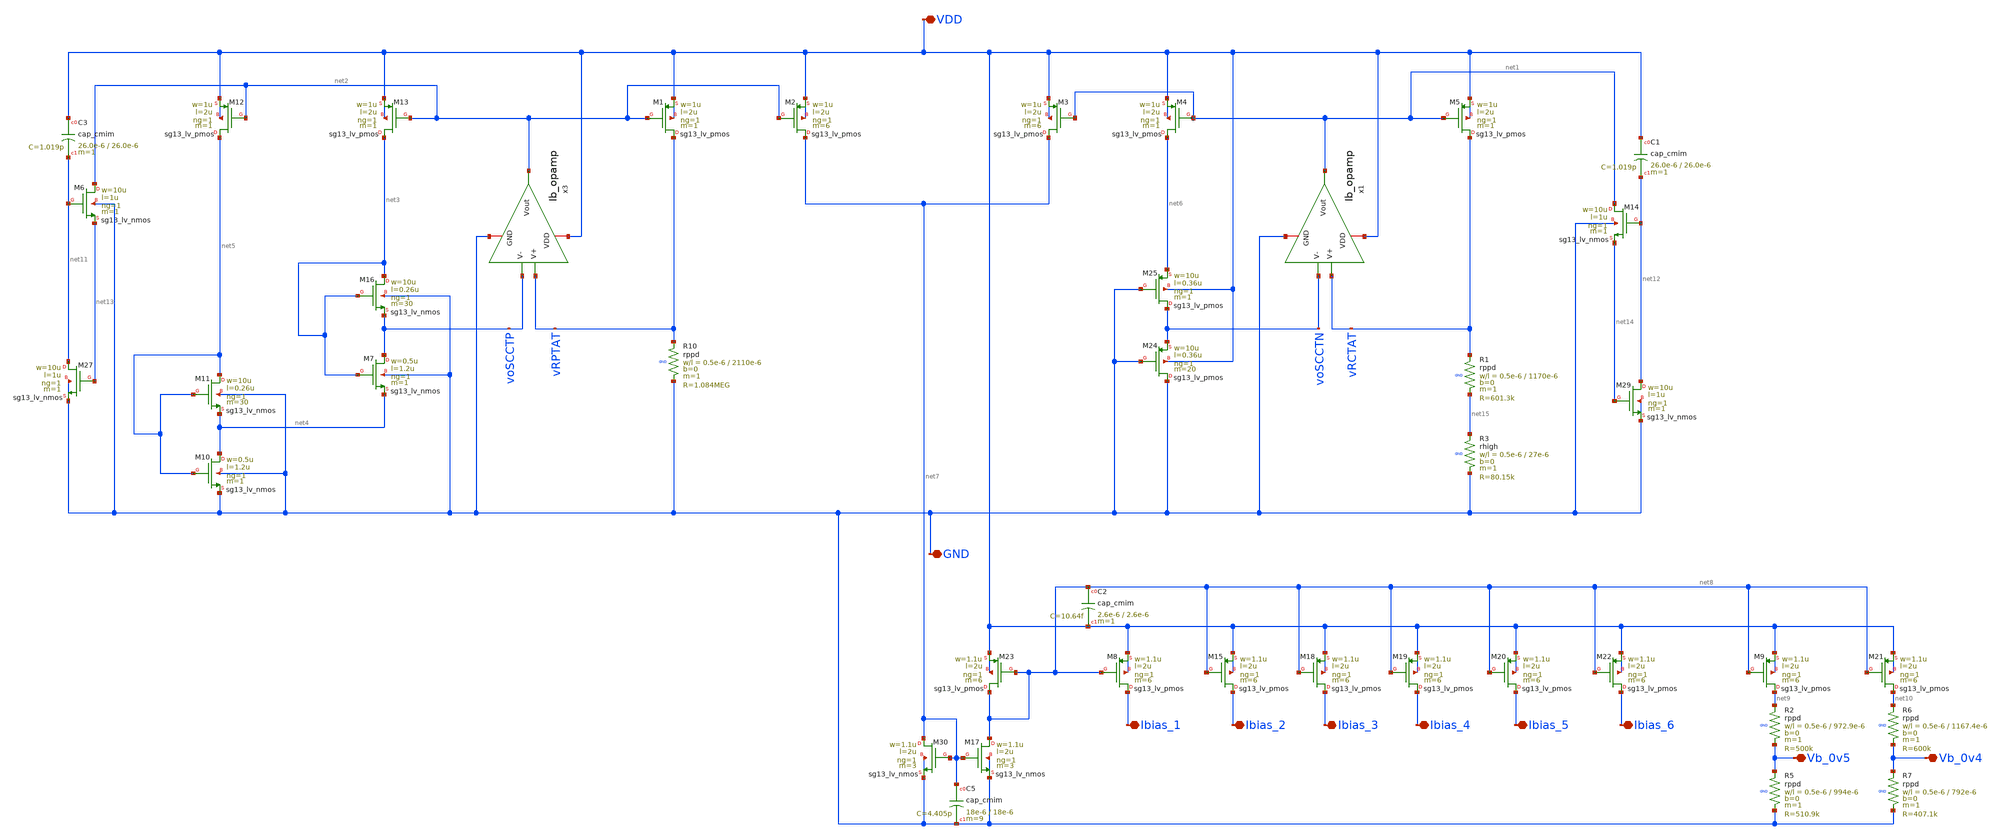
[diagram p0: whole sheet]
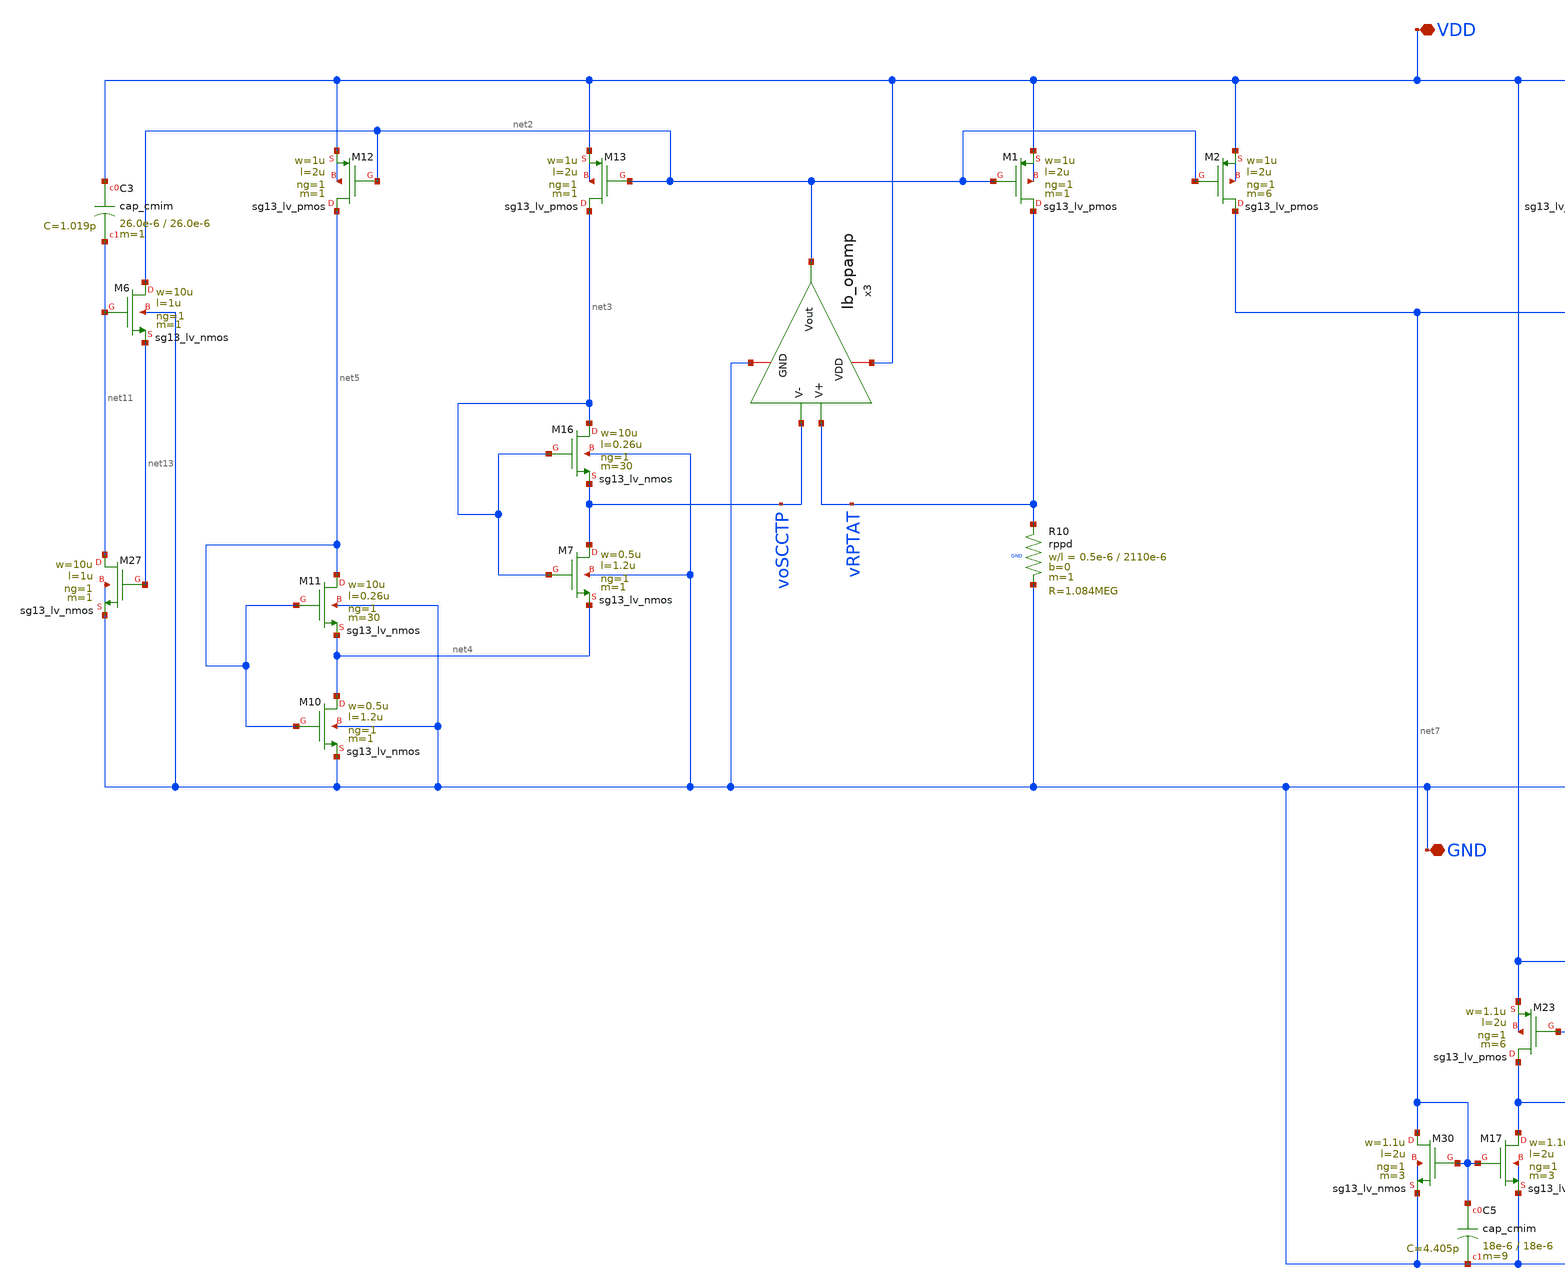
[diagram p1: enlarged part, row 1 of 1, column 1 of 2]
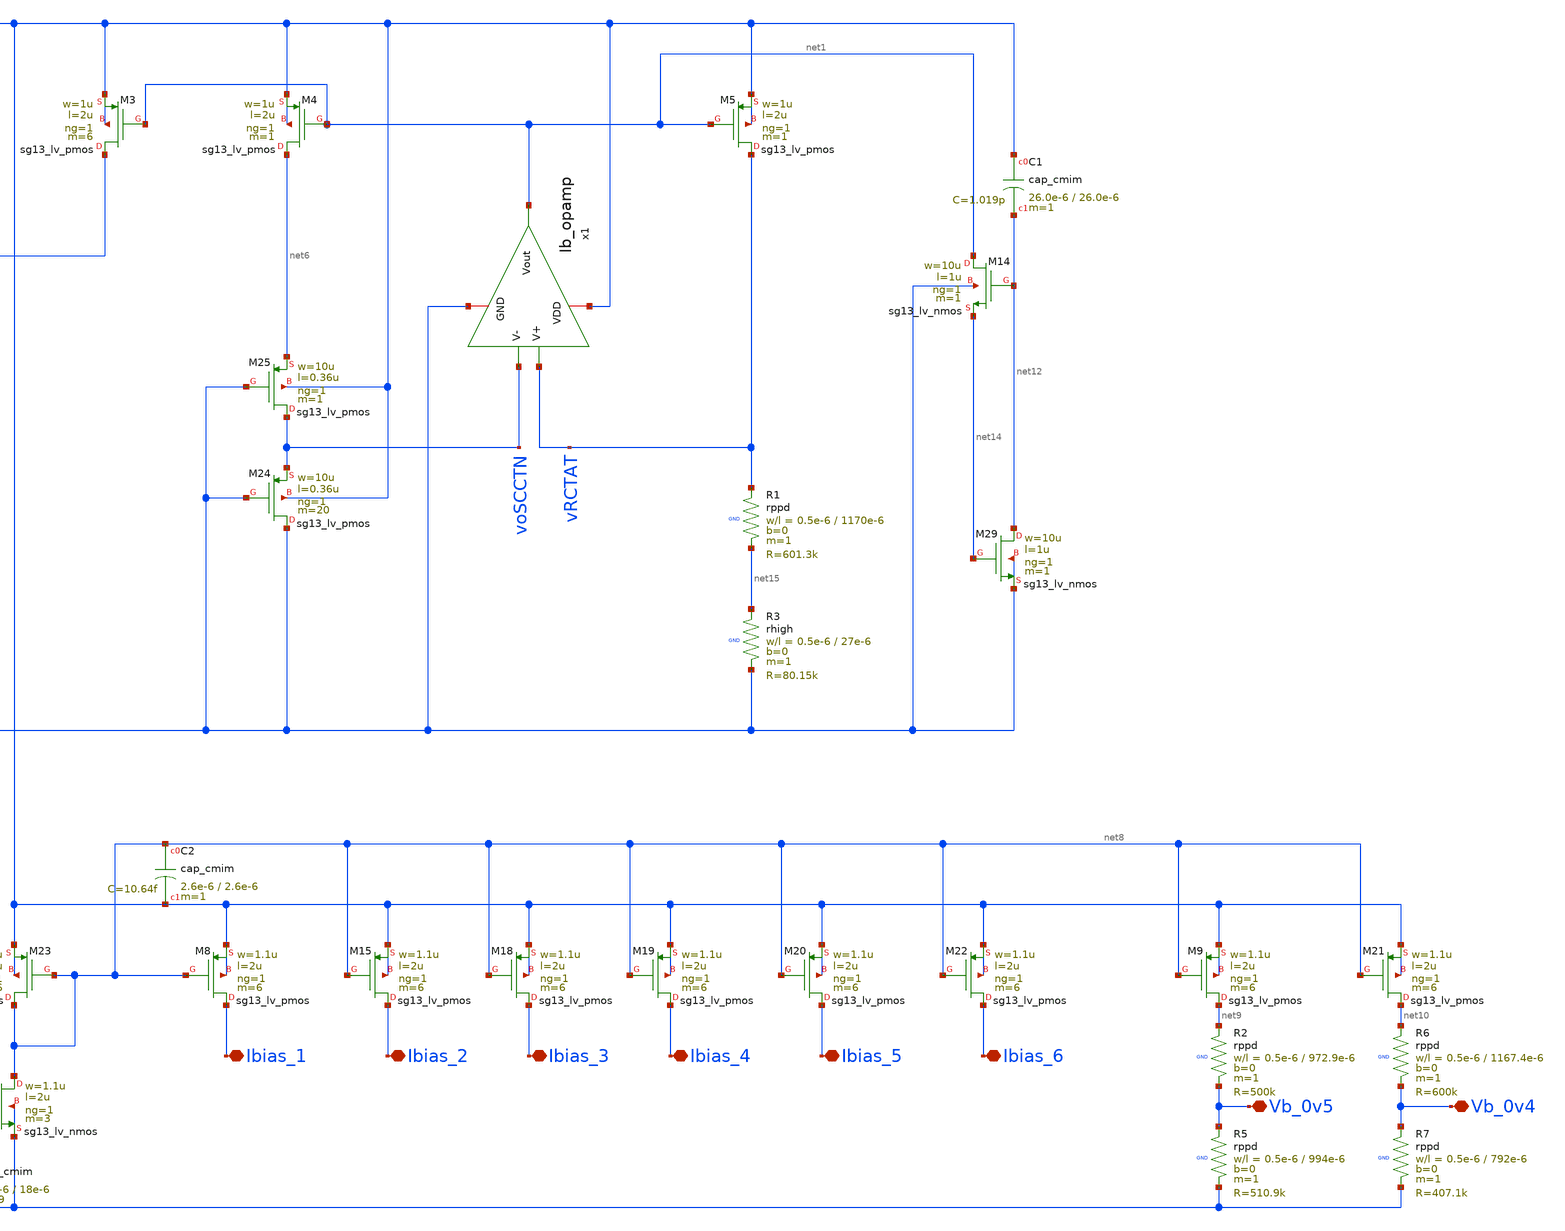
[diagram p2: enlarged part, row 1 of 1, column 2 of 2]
** sch_path: SSDOR_1.2V_v3/components/Ibias_uA/CTAT_PTAT/CTAT_PTAT.sch
**.subckt CTAT_PTAT VDD GND Ibias_1 Ibias_2 Ibias_3 Ibias_4 Ibias_5 Ibias_6 Vb_0v4 Vb_0v5
*.iopin VDD
*.iopin GND
*.iopin Ibias_1
*.iopin Ibias_2
*.iopin Ibias_3
*.iopin Ibias_4
*.iopin Ibias_5
*.iopin Ibias_6
*.iopin Vb_0v4
*.iopin Vb_0v5
XM1 vRPTAT net2 VDD VDD sg13_lv_pmos w=1u l=2u ng=1 m=1 mm_ok=1
XM2 net7 net2 VDD VDD sg13_lv_pmos w=1u l=2u ng=1 m=6 mm_ok=1
XM3 net7 net1 VDD VDD sg13_lv_pmos w=1u l=2u ng=1 m=6 mm_ok=1
XM4 net6 net1 VDD VDD sg13_lv_pmos w=1u l=2u ng=1 m=1 mm_ok=1
XM12 net5 net2 VDD VDD sg13_lv_pmos w=1u l=2u ng=1 m=1 mm_ok=1
XM13 net3 net2 VDD VDD sg13_lv_pmos w=1u l=2u ng=1 m=1 mm_ok=1
XM5 vRCTAT net1 VDD VDD sg13_lv_pmos w=1u l=2u ng=1 m=1 mm_ok=1
XM7 voSCCTP net3 net4 GND sg13_lv_nmos w=0.5u l=1.2u ng=1 m=1 mm_ok=1
XM10 net4 net5 GND GND sg13_lv_nmos w=0.5u l=1.2u ng=1 m=1 mm_ok=1
XM11 net5 net5 net4 GND sg13_lv_nmos w=10u l=0.26u ng=1 m=30 mm_ok=1
XM16 net3 net3 voSCCTP GND sg13_lv_nmos w=10u l=0.26u ng=1 m=30 mm_ok=1
XM30 net7 net7 GND GND sg13_lv_nmos w=1.1u l=2u ng=1 m=3 mm_ok=1
XR2 net9 Vb_0v5 GND rppd w=0.5e-6 l=972.9e-6 m=1 b=0 mm_ok=1
XR6 net10 Vb_0v4 GND rppd w=0.5e-6 l=1167.4e-6 m=1 b=0 mm_ok=1
XR7 Vb_0v4 GND GND rppd w=0.5e-6 l=792e-6 m=1 b=0 mm_ok=1
XR5 Vb_0v5 GND GND rppd w=0.5e-6 l=994e-6 m=1 b=0 mm_ok=1
XM17 net8 net7 GND GND sg13_lv_nmos w=1.1u l=2u ng=1 m=3 mm_ok=1
XM23 net8 net8 VDD VDD sg13_lv_pmos w=1.1u l=2u ng=1 m=6 mm_ok=1
XM8 Ibias_1 net8 VDD VDD sg13_lv_pmos w=1.1u l=2u ng=1 m=6 mm_ok=1
XM15 Ibias_2 net8 VDD VDD sg13_lv_pmos w=1.1u l=2u ng=1 m=6 mm_ok=1
XM18 Ibias_3 net8 VDD VDD sg13_lv_pmos w=1.1u l=2u ng=1 m=6 mm_ok=1
XM19 Ibias_4 net8 VDD VDD sg13_lv_pmos w=1.1u l=2u ng=1 m=6 mm_ok=1
XM20 Ibias_5 net8 VDD VDD sg13_lv_pmos w=1.1u l=2u ng=1 m=6 mm_ok=1
XM22 Ibias_6 net8 VDD VDD sg13_lv_pmos w=1.1u l=2u ng=1 m=6 mm_ok=1
XM24 GND GND voSCCTN VDD sg13_lv_pmos w=10u l=0.36u ng=1 m=20 mm_ok=1
XM25 voSCCTN GND net6 VDD sg13_lv_pmos w=10u l=0.36u ng=1 m=1 mm_ok=1
XM27 net11 net13 GND GND sg13_lv_nmos w=10u l=1u ng=1 m=1 mm_ok=1
XM29 net12 net14 GND GND sg13_lv_nmos w=10u l=1u ng=1 m=1 mm_ok=1
XR1 vRCTAT net15 GND rppd w=0.5e-6 l=1170e-6 m=1 b=0 mm_ok=1
XR3 net15 GND GND rhigh w=0.5e-6 l=27e-6 m=1 b=0 mm_ok=1
XR10 vRPTAT GND GND rppd w=0.5e-6 l=2110e-6 m=1 b=0 mm_ok=1
XC3 VDD net11 cap_cmim w=26.0e-6 l=26.0e-6 m=1 mm_ok=1
XC1 VDD net12 cap_cmim w=26.0e-6 l=26.0e-6 m=1 mm_ok=1
XM6 net2 net11 net13 GND sg13_lv_nmos w=10u l=1u ng=1 m=1 mm_ok=1
XM14 net1 net12 net14 GND sg13_lv_nmos w=10u l=1u ng=1 m=1 mm_ok=1
x3 VDD net2 voSCCTP vRPTAT GND Ib_opamp
x1 VDD net1 voSCCTN vRCTAT GND Ib_opamp
XC5 net7 GND cap_cmim w=18e-6 l=18e-6 m=9 mm_ok=1
XC2 net8 VDD cap_cmim w=2.6e-6 l=2.6e-6 m=1 mm_ok=1
XM9 net9 net8 VDD VDD sg13_lv_pmos w=1.1u l=2u ng=1 m=6 mm_ok=1
XM21 net10 net8 VDD VDD sg13_lv_pmos w=1.1u l=2u ng=1 m=6 mm_ok=1
**.ends
.end
